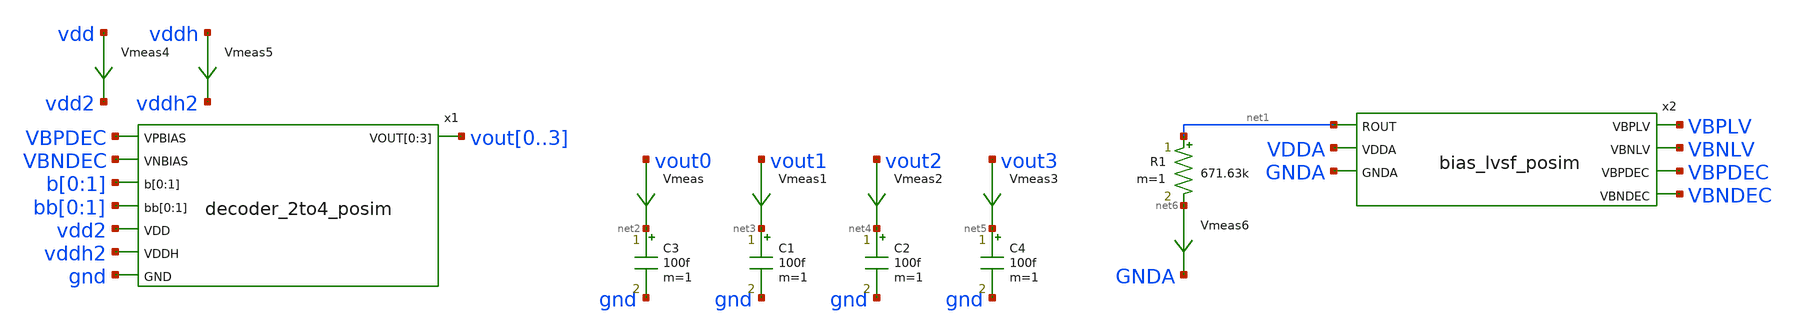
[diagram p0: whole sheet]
** sch_path: xschem/decoder_2to4-tb.sch
.lib $::SKYWATER_MODELS/sky130.lib.spice tt
.include $::SKYWATER_STDCELLS/sky130_fd_sc_hd.spice

**.subckt decoder_2to4-tb
Vmeas vout0 net2 0
.save i(vmeas)
Vmeas1 vout1 net3 0
.save i(vmeas1)
C3 net2 gnd 100f m=1
Vmeas2 vout2 net4 0
.save i(vmeas2)
Vmeas3 vout3 net5 0
.save i(vmeas3)
C1 net3 gnd 100f m=1
C2 net4 gnd 100f m=1
C4 net5 gnd 100f m=1
Vmeas4 vdd vdd2 0
.save i(vmeas4)
Vmeas5 vddh vddh2 0
.save i(vmeas5)
Vmeas6 net6 GNDA 0
.save i(vmeas6)
x1 VBPDEC VBNDEC b[0] b[1] bb[0] bb[1] vout0 vout1 vout2 vout3 vdd2 vddh2 gnd decoder_2to4_posim
x2 net1 VBPLV VBNLV VBPDEC VBNDEC VDDA GNDA bias_lvsf_posim
R1 net1 net6 671.63k m=1
**** begin user architecture code


.include $THESIS_WS/spice/decoder_2to4-tb.sp

**** end user architecture code
**.ends
.end
